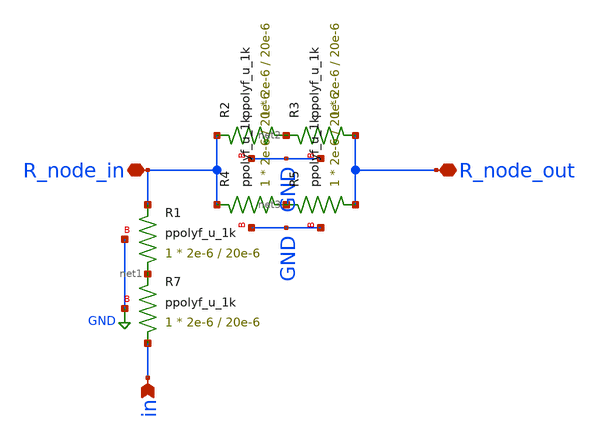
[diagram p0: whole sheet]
** sch_path: xschem/dac_sub_r2r.sch
**.subckt dac_sub_r2r in R_node_out R_node_in
*.ipin in
*.iopin R_node_out
*.iopin R_node_in
XR7 in net1 GND ppolyf_u_1k r_width=2e-6 r_length=20e-6 m=1
XR1 net1 R_node_in GND ppolyf_u_1k r_width=2e-6 r_length=20e-6 m=1
XR2 net2 R_node_in GND ppolyf_u_1k r_width=2e-6 r_length=20e-6 m=1
XR3 R_node_out net2 GND ppolyf_u_1k r_width=2e-6 r_length=20e-6 m=1
XR4 net3 R_node_in GND ppolyf_u_1k r_width=2e-6 r_length=20e-6 m=1
XR5 R_node_out net3 GND ppolyf_u_1k r_width=2e-6 r_length=20e-6 m=1
**.ends
.GLOBAL GND
.end
